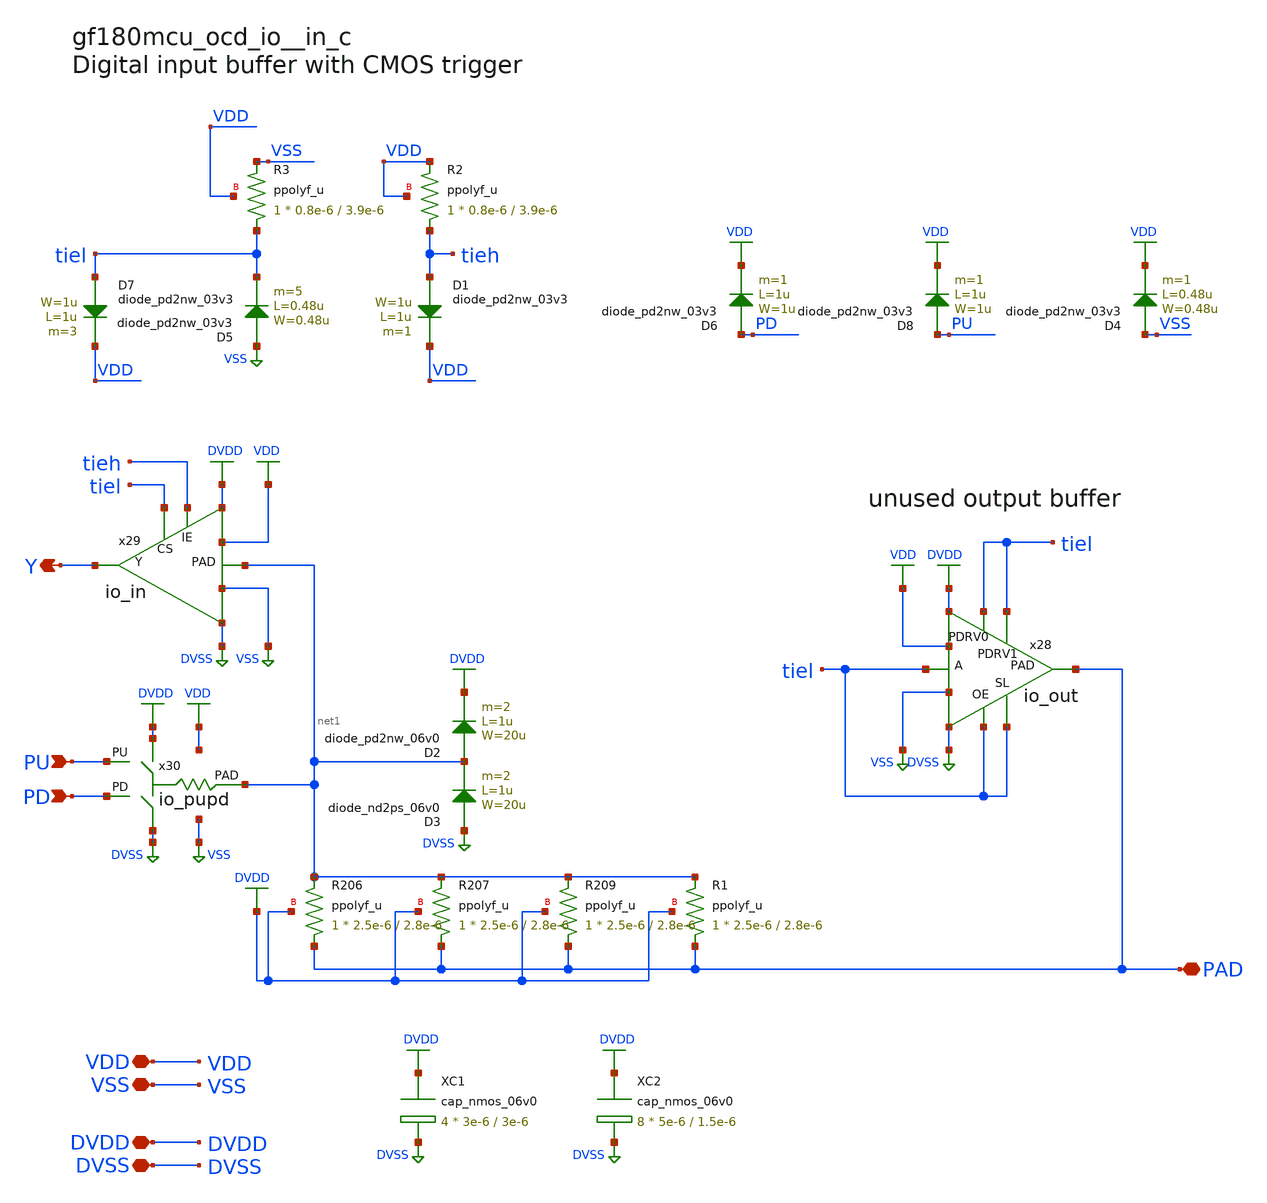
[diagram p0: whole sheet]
** sch_path: cells/in_c/gf180mcu_ocd_io__in_c.sch
* Copyright 2023 David Mitchell Bailey
* Licensed under the Apache License, Version 2.0 (the "License");
* you may not use this file except in compliance with the License.
* You may obtain a copy of the License at
* https://www.apache.org/licenses/LICENSE-2.0
* Unless required by applicable law or agreed to in writing, software
* distributed under the License is distributed on an "AS IS" BASIS,
* WITHOUT WARRANTIES OR CONDITIONS OF ANY KIND, either express or implied.
* See the License for the specific language governing permissions and
* limitations under the License.
**.subckt gf180mcu_ocd_io__in_c VDD Y VSS DVDD DVSS PU PD PAD
*.iopin VDD
*.opin Y
*.iopin VSS
*.iopin DVDD
*.iopin DVSS
*.ipin PU
*.ipin PD
*.iopin PAD
XR206 PAD net1 DVDD ppolyf_u r_width=2.5e-6 r_length=2.8e-6 m=1
XR207 PAD net1 DVDD ppolyf_u r_width=2.5e-6 r_length=2.8e-6 m=1
XR209 PAD net1 DVDD ppolyf_u r_width=2.5e-6 r_length=2.8e-6 m=1
XR1 PAD net1 DVDD ppolyf_u r_width=2.5e-6 r_length=2.8e-6 m=1
x28 tiel tiel tiel tiel tiel PAD DVDD DVSS VDD VSS io_out
x29 net1 tieh tiel Y DVDD DVSS VDD VSS io_in
x30 DVDD DVSS PU PD net1 VDD VSS io_pupd
XC1 DVDD DVSS cap_nmos_06v0 c_width=3e-6 c_length=3e-6 m=4
XC2 DVDD DVSS cap_nmos_06v0 c_width=5e-6 c_length=1.5e-6 m=8
D3 DVSS net1 diode_nd2ps_06v0 area='20u * 1u ' pj='2*20u + 2*1u ' m=2
D2 net1 DVDD diode_pd2nw_06v0 area='20u * 1u ' pj='2*20u + 2*1u ' m=2
XR2 tieh VDD VDD ppolyf_u r_width=0.8e-6 r_length=3.9e-6 m=1
XR3 tiel VSS VDD ppolyf_u r_width=0.8e-6 r_length=3.9e-6 m=1
D7 tiel VDD diode_pd2nw_03v3 area='1u * 1u ' pj='2*1u + 2*1u ' m=3
D5 VSS tiel diode_pd2nw_03v3 area='0.48u * 0.48u ' pj='2*0.48u + 2*0.48u ' m=5
D1 tieh VDD diode_pd2nw_03v3 area='1u * 1u ' pj='2*1u + 2*1u ' m=1
D6 PD VDD diode_pd2nw_03v3 area='1u * 1u ' pj='2*1u + 2*1u ' m=1
D8 PU VDD diode_pd2nw_03v3 area='1u * 1u ' pj='2*1u + 2*1u ' m=1
D4 VSS VDD diode_pd2nw_03v3 area='0.48u * 0.48u ' pj='2*0.48u + 2*0.48u ' m=1
**.ends
.GLOBAL DVSS
.GLOBAL DVDD
.GLOBAL VDD
.GLOBAL VSS
.end
